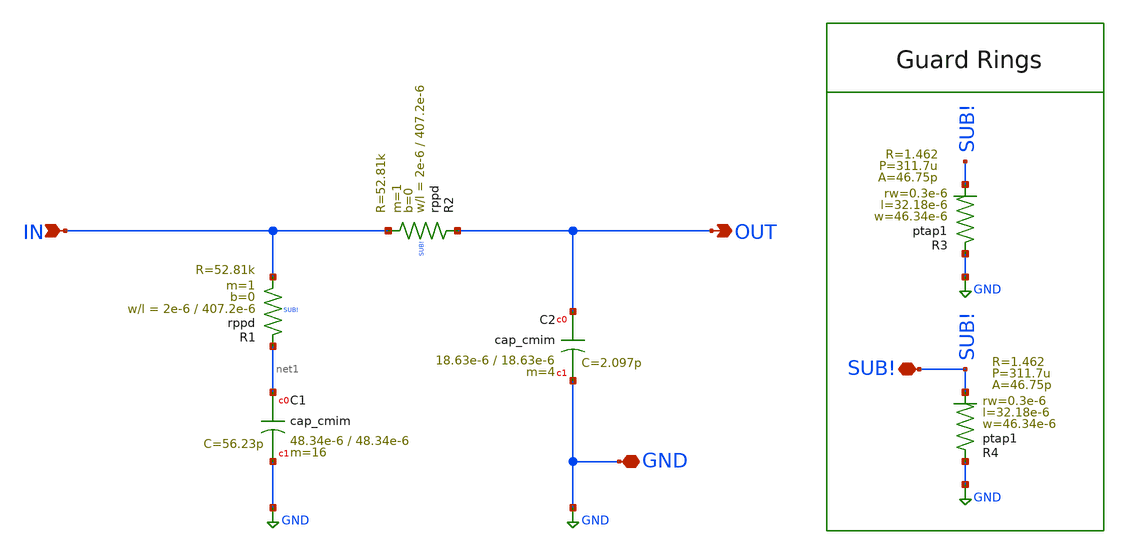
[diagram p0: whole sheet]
** sch_path: xschem/loop-filter/LOOP_FILTER.sch
**.subckt LOOP_FILTER OUT GND IN SUB!
*.opin OUT
*.iopin GND
*.ipin IN
*.iopin SUB!
XC2 OUT GND cap_cmim w=18.63e-6 l=18.63e-6 m=4 mm_ok=1
XC1 net1 GND cap_cmim w=48.34e-6 l=48.34e-6 m=16 mm_ok=1
XR2 OUT IN SUB! rppd w=2e-6 l=407.2e-6 m=1 b=0 mm_ok=1
XR1 net1 IN SUB! rppd w=2e-6 l=407.2e-6 m=1 b=0 mm_ok=1
XR3 GND SUB! ptap1 R=1.462 w=46.34e-6 l=32.18e-6 rw=0.3e-6
XR4 GND SUB! ptap1 R=1.462 w=46.34e-6 l=32.18e-6 rw=0.3e-6
**.ends
.GLOBAL GND
.end
